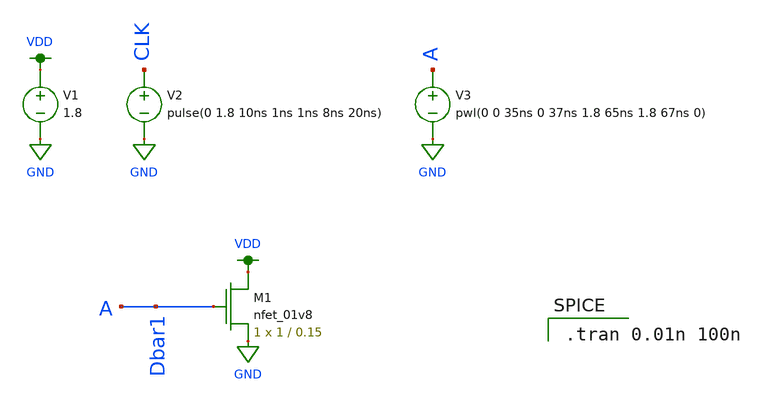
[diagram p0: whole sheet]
** sch_path: mp2/xschem/flipflop/test_cases/flipflop_test_1.sch
**.subckt flipflop_test_1
V1 VDD GND 1.8
V2 CLK GND pulse(0 1.8 10ns 1ns 1ns 8ns 20ns)
V3 A GND pwl(0 0 35ns 0 37ns 1.8 65ns 1.8 67ns 0)
XM1 VDD A GND GND sky130_fd_pr__nfet_01v8 L=0.15 W=1 nf=1 ad='int((nf+1)/2) * W/nf * 0.29' as='int((nf+2)/2) * W/nf * 0.29'
+ pd='2*int((nf+1)/2) * (W/nf + 0.29)' ps='2*int((nf+2)/2) * (W/nf + 0.29)' nrd='0.29 / W' nrs='0.29 / W'
+ sa=0 sb=0 sd=0 mult=1 m=1
**** begin user architecture code

.option wnflag=1
.lib ~/skywater/skywater-pdk/libraries/sky130_fd_pr_ngspice/latest/models/sky130.lib.spice tt


.tran 0.01n 100n

**** end user architecture code
**.ends
.GLOBAL VDD
.GLOBAL GND
.end
